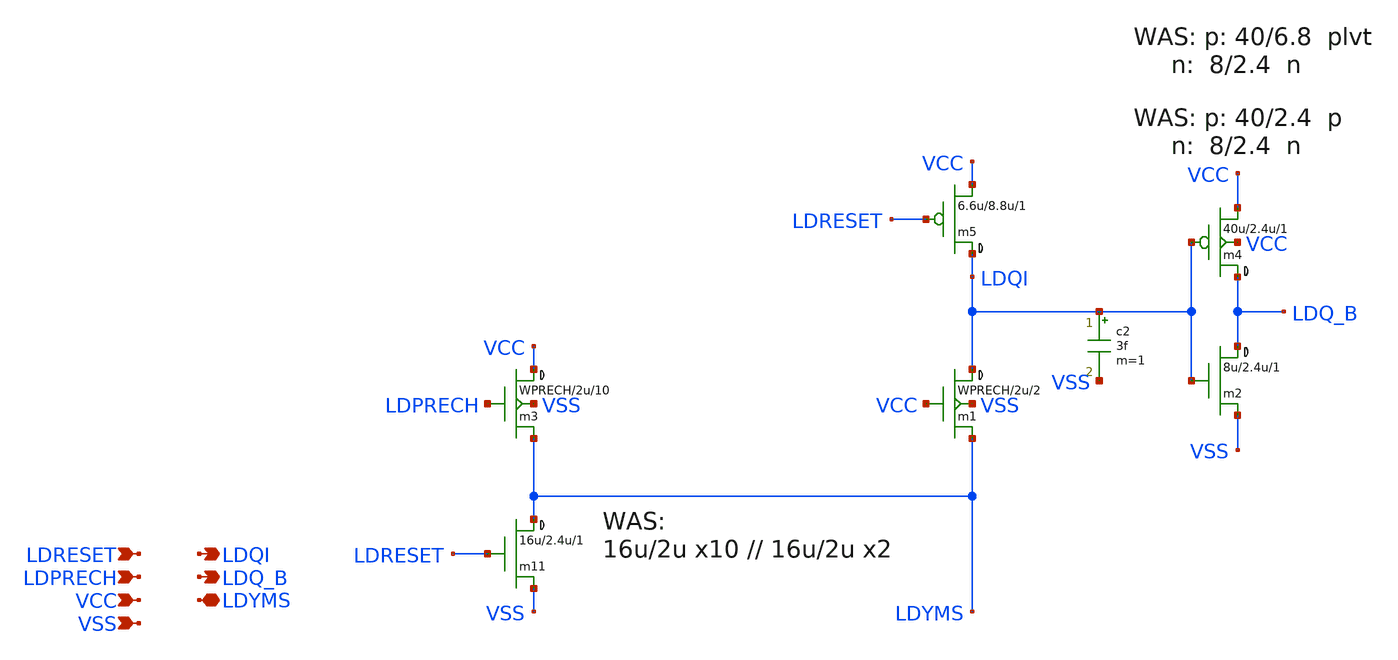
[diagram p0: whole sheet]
** sch_path: xschem_libs_newsym/rom8k/rom2_sacell/schematic/rom2_sacell.sch
* Copyright (C) 1998-2024 Stefan Frederik Schippers
* This program is free software; you can redistribute it and/or modify
* it under the terms of the GNU General Public License as published by
* the Free Software Foundation; either version 2 of the License, or
* (at your option) any later version.
* This program is distributed in the hope that it will be useful,
* but WITHOUT ANY WARRANTY; without even the implied warranty of
* MERCHANTABILITY or FITNESS FOR A PARTICULAR PURPOSE.  See the
* GNU General Public License for more details.
* You should have received a copy of the GNU General Public License
* along with this program; if not, write to the Free Software
**.subckt rom2_sacell LDRESET LDPRECH VCC VSS LDQI LDQ_B LDYMS
*.ipin LDRESET
*.ipin LDPRECH
*.ipin VCC
*.ipin VSS
*.opin LDQI
*.opin LDQ_B
*.iopin LDYMS
m3 VCC LDPRECH LDYMS VSS cmosn w=WPRECH l=2u ad='WPRECH *4.3u' as='WPRECH *4.3u' pd='WPRECH *2+8.6u'
+ ps='WPRECH *2+8.6u' m=10
m1 LDQI VCC LDYMS VSS cmosn w=WPRECH l=2u ad='WPRECH *4.3u' as='WPRECH *4.3u' pd='WPRECH *2+8.6u' ps='WPRECH *2+8.6u'
+ m=2
m5 LDQI LDRESET VCC VCC cmosp w=6.6u l=8.8u ad={6.6u *4.4u} as={6.6u *4.4u} pd={6.6u *2 + 8.8u} ps={6.6u *2 + 8.8u}
+ m=1
m11 LDYMS LDRESET VSS 0 cmosn w=16u l=2.4u ad={16u *4.4u} as={16u *4.4u} pd={16u *2 + 8.8u} ps={16u *2 + 8.8u}
+ m=1
c2 LDQI VSS 3f m=1
m2 LDQ_B LDQI VSS 0 cmosn w=8u l=2.4u ad={8u *4.4u} as={8u *4.4u} pd={8u *2 + 8.8u} ps={8u *2 + 8.8u}
+ m=1
m4 LDQ_B LDQI VCC VCC cmosp w=40u l=2.4u ad='40u *4.6u' as='40u *4.6u' pd='40u *2+9.2u' ps='40u *2+9.2u'
+ m=1
**.ends
.end
